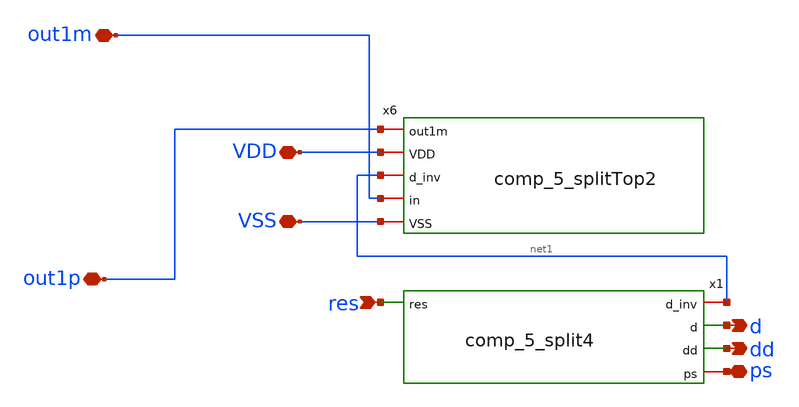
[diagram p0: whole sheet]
** sch_path: 5_Design/4_Layout/Team 5/splitUpSimulationsAndSchematics/comp_5_splitTop4.sch
**.subckt comp_5_splitTop4 res dd d out1m out1p VDD VSS ps
*.ipin res
*.opin dd
*.opin d
*.iopin out1m
*.iopin out1p
*.iopin VDD
*.iopin VSS
*.iopin ps
x6 out1p VDD net1 out1m VSS comp_5_splitTop2
x1 net1 d dd ps res comp_5_split4
**.ends
.end
